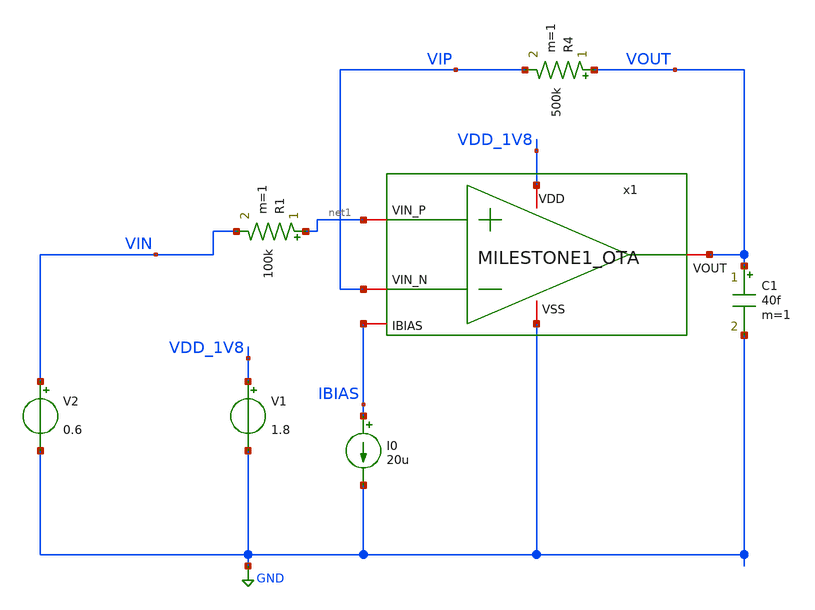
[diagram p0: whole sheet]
** sch_path: design/CNR_GR03_SKY130NM/MILESTONE1_OTA_TB.sch
**.subckt MILESTONE1_OTA_TB
V1 VDD_1V8 GND 1.8
I0 IBIAS GND 20u
C1 VOUT GND 40f m=1
V2 VIN GND 0.6
R4 VOUT VIP 500k m=1
R1 net1 VIN 100k m=1
x1 VDD_1V8 IBIAS VOUT net1 VIP GND MILESTONE1_OTA
**** begin user architecture code



* ngspice commands
.include corner.spi



**** end user architecture code
**.ends
.GLOBAL GND
.end
